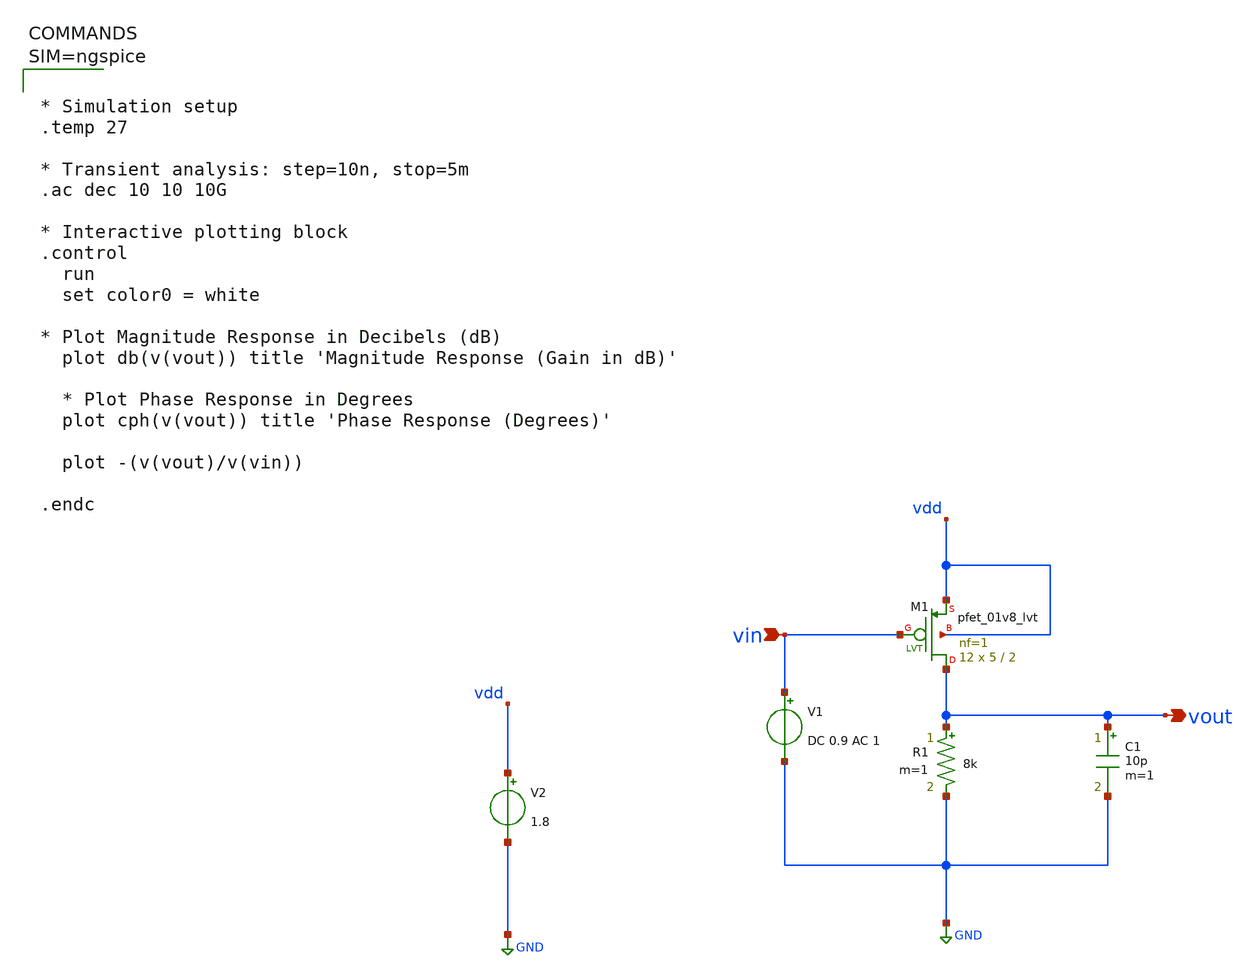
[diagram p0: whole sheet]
** sch_path: testbenches/PMOS_res_load_DBGain.sch
**.subckt PMOS_res_load_DBGain vin vout
*.ipin vin
*.opin vout
XM1 vout vin vdd vdd sky130_fd_pr__pfet_01v8_lvt L=2 W=5 nf=1 ad='int((1 + 1)/2) * 5 / 1 * 0.29' as='int((1 + 2)/2) * 5 / 1 * 0.29'
+ pd='2*int((1 + 1)/2) * (5 / 1 + 0.29)' ps='2*int((1 + 2)/2) * (5 / 1 + 0.29)' nrd='0.29 / 5 ' nrs='0.29 / 5 '
+ sa=0 sb=0 sd=0 mult=12 m=12
R1 vout GND 8k m=1
V1 vin GND DC 0.9 AC 1
C1 vout GND 10p m=1
V2 vdd GND 1.8
**** begin user architecture code

** opencircuitdesign pdks install
.lib $::SKYWATER_MODELS/sky130.lib.spice tt




* Simulation setup
.temp 27

* Transient analysis: step=10n, stop=5m
.ac dec 10 10 10G

* Interactive plotting block
.control
  run
  set color0 = white

* Plot Magnitude Response in Decibels (dB)
  plot db(v(vout)) title 'Magnitude Response (Gain in dB)'

  * Plot Phase Response in Degrees
  plot cph(v(vout)) title 'Phase Response (Degrees)'

  plot -(v(vout)/v(vin))

.endc




**** end user architecture code
**.ends
.GLOBAL GND
.end
